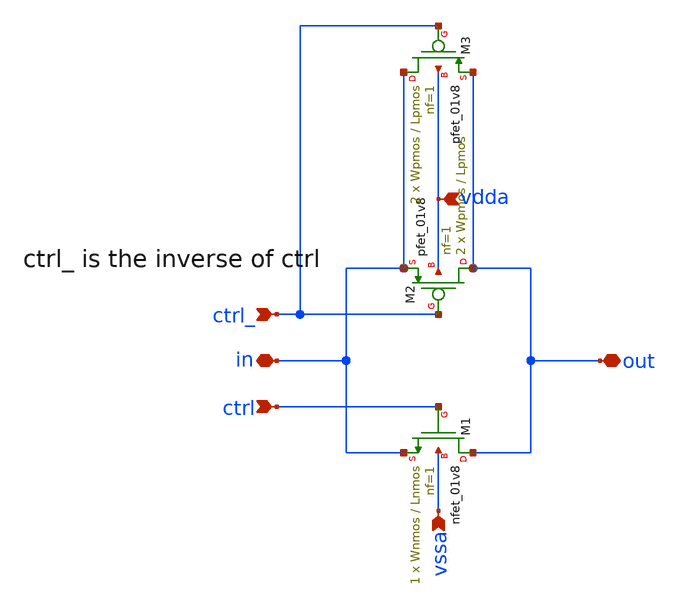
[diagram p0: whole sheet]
** sch_path: xschem/transmission_gate/transmission_gate.sch
**.subckt transmission_gate in out ctrl_ ctrl vdda vssa
*.iopin in
*.iopin out
*.ipin ctrl_
*.ipin ctrl
*.ipin vdda
*.ipin vssa
XM1 out ctrl in vssa sky130_fd_pr__nfet_01v8 L=Lnmos W=Wnmos nf=1 ad='int((nf+1)/2) * W/nf * 0.29' as='int((nf+2)/2) * W/nf * 0.29'
+ pd='2*int((nf+1)/2) * (W/nf + 0.29)' ps='2*int((nf+2)/2) * (W/nf + 0.29)' nrd='0.29 / W' nrs='0.29 / W'
+ sa=0 sb=0 sd=0 mult=1 m=1
XM2 out ctrl_ in vdda sky130_fd_pr__pfet_01v8 L=Lpmos W=Wpmos nf=1 ad='int((nf+1)/2) * W/nf * 0.29' as='int((nf+2)/2) * W/nf * 0.29'
+ pd='2*int((nf+1)/2) * (W/nf + 0.29)' ps='2*int((nf+2)/2) * (W/nf + 0.29)' nrd='0.29 / W' nrs='0.29 / W'
+ sa=0 sb=0 sd=0 mult=2 m=2
XM3 in ctrl_ out vdda sky130_fd_pr__pfet_01v8 L=Lpmos W=Wpmos nf=1 ad='int((nf+1)/2) * W/nf * 0.29' as='int((nf+2)/2) * W/nf * 0.29'
+ pd='2*int((nf+1)/2) * (W/nf + 0.29)' ps='2*int((nf+2)/2) * (W/nf + 0.29)' nrd='0.29 / W' nrs='0.29 / W'
+ sa=0 sb=0 sd=0 mult=2 m=2
**.ends
.end
